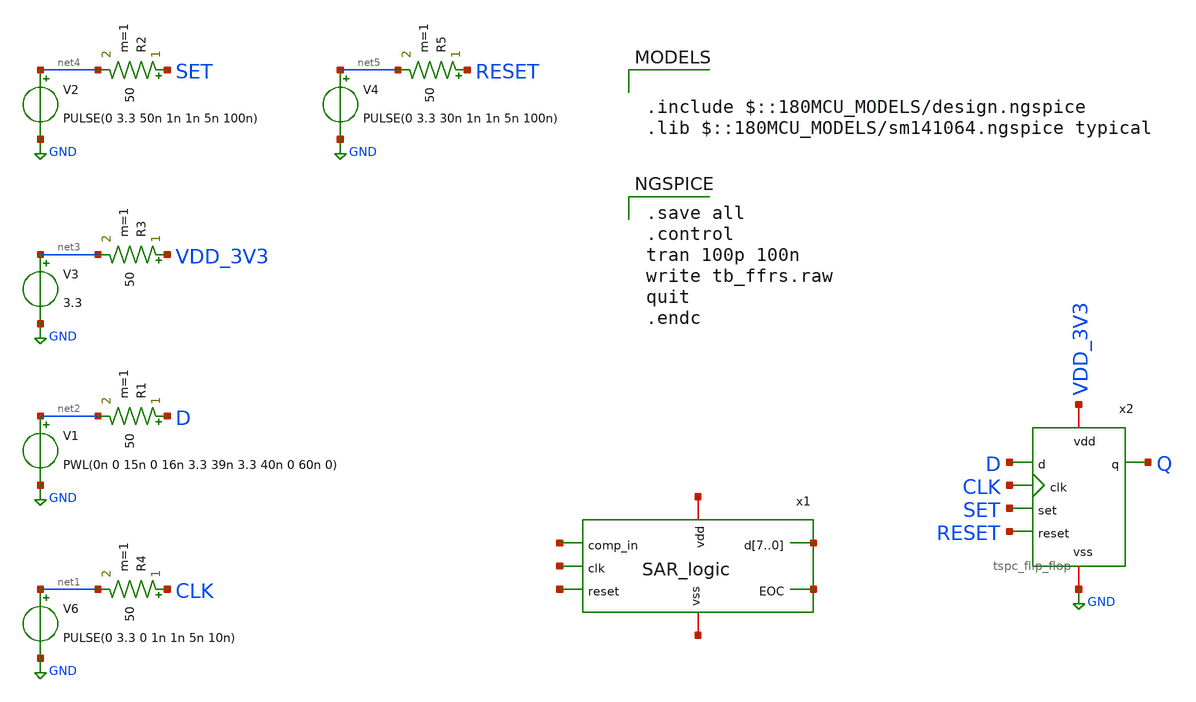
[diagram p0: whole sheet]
** sch_path: designs/libs/SAR_logic/SAR_logic_tb.sch
**.subckt SAR_logic_tb
V6 net1 GND PULSE(0 3.3 0 1n 1n 5n 10n)
R4 CLK net1 50 m=1
V1 net2 GND PWL(0n 0 15n 0 16n 3.3 39n 3.3 40n 0 60n 0)
R1 D net2 50 m=1
V3 net3 GND 3.3
R3 VDD_3V3 net3 50 m=1
V2 net4 GND PULSE(0 3.3 50n 1n 1n 5n 100n)
R2 SET net4 50 m=1
V4 net5 GND PULSE(0 3.3 30n 1n 1n 5n 100n)
R5 RESET net5 50 m=1
x2 VDD_3V3 GND D CLK SET RESET Q tspc_flip_flop
x1 net6 net7[7] net7[6] net7[5] net7[4] net7[3] net7[2] net7[1] net7[0] net8 net9 net10 net11 net12
+ SAR_logic
**** begin user architecture code

.include $::180MCU_MODELS/design.ngspice
.lib $::180MCU_MODELS/sm141064.ngspice typical


.save all
.control
tran 100p 100n
write tb_ffrs.raw
quit
.endc

**** end user architecture code
**.ends

* expanding   symbol:  libs/tspc_flip_flop/tspc_flip_flop.sym # of pins=7
** sym_path: designs/libs/tspc_flip_flop/tspc_flip_flop.sym
** sch_path: designs/libs/tspc_flip_flop/tspc_flip_flop.sch
.subckt tspc_flip_flop vdd vss d clk set reset q
*.iopin vdd
*.iopin vss
*.ipin d
*.ipin clk
*.ipin set
*.ipin reset
*.opin q
XM1 b1 d vss vss nfet_03v3 L=0.28u W=1u nf=1 ad='int((nf+1)/2) * W/nf * 0.18u' as='int((nf+2)/2) * W/nf * 0.18u'
+ pd='2*int((nf+1)/2) * (W/nf + 0.18u)' ps='2*int((nf+2)/2) * (W/nf + 0.18u)' nrd='0.18u / W' nrs='0.18u / W'
+ sa=0 sb=0 sd=0 m=1
XM2 b1 clk net1 net1 pfet_03v3 L=0.28u W=2u nf=1 ad='int((nf+1)/2) * W/nf * 0.18u' as='int((nf+2)/2) * W/nf * 0.18u'
+ pd='2*int((nf+1)/2) * (W/nf + 0.18u)' ps='2*int((nf+2)/2) * (W/nf + 0.18u)' nrd='0.18u / W' nrs='0.18u / W'
+ sa=0 sb=0 sd=0 m=1
XM3 net1 d vdd vdd pfet_03v3 L=0.28u W=2u nf=1 ad='int((nf+1)/2) * W/nf * 0.18u' as='int((nf+2)/2) * W/nf * 0.18u'
+ pd='2*int((nf+1)/2) * (W/nf + 0.18u)' ps='2*int((nf+2)/2) * (W/nf + 0.18u)' nrd='0.18u / W' nrs='0.18u / W'
+ sa=0 sb=0 sd=0 m=1
XM4 b2 clk vdd vdd pfet_03v3 L=0.28u W=2u nf=1 ad='int((nf+1)/2) * W/nf * 0.18u' as='int((nf+2)/2) * W/nf * 0.18u'
+ pd='2*int((nf+1)/2) * (W/nf + 0.18u)' ps='2*int((nf+2)/2) * (W/nf + 0.18u)' nrd='0.18u / W' nrs='0.18u / W'
+ sa=0 sb=0 sd=0 m=1
XM5 b2 b1 net2 vss nfet_03v3 L=0.28u W=1u nf=1 ad='int((nf+1)/2) * W/nf * 0.18u' as='int((nf+2)/2) * W/nf * 0.18u'
+ pd='2*int((nf+1)/2) * (W/nf + 0.18u)' ps='2*int((nf+2)/2) * (W/nf + 0.18u)' nrd='0.18u / W' nrs='0.18u / W'
+ sa=0 sb=0 sd=0 m=1
XM6 net2 clk vss vss nfet_03v3 L=0.28u W=1u nf=1 ad='int((nf+1)/2) * W/nf * 0.18u' as='int((nf+2)/2) * W/nf * 0.18u'
+ pd='2*int((nf+1)/2) * (W/nf + 0.18u)' ps='2*int((nf+2)/2) * (W/nf + 0.18u)' nrd='0.18u / W' nrs='0.18u / W'
+ sa=0 sb=0 sd=0 m=1
XM7 net4 b2 vss vss nfet_03v3 L=0.28u W=1u nf=1 ad='int((nf+1)/2) * W/nf * 0.18u' as='int((nf+2)/2) * W/nf * 0.18u'
+ pd='2*int((nf+1)/2) * (W/nf + 0.18u)' ps='2*int((nf+2)/2) * (W/nf + 0.18u)' nrd='0.18u / W' nrs='0.18u / W'
+ sa=0 sb=0 sd=0 m=1
XM8 b3 clk net4 vss nfet_03v3 L=0.28u W=1u nf=1 ad='int((nf+1)/2) * W/nf * 0.18u' as='int((nf+2)/2) * W/nf * 0.18u'
+ pd='2*int((nf+1)/2) * (W/nf + 0.18u)' ps='2*int((nf+2)/2) * (W/nf + 0.18u)' nrd='0.18u / W' nrs='0.18u / W'
+ sa=0 sb=0 sd=0 m=1
XM9 b3 set net3 net3 pfet_03v3 L=0.28u W=2u nf=1 ad='int((nf+1)/2) * W/nf * 0.18u' as='int((nf+2)/2) * W/nf * 0.18u'
+ pd='2*int((nf+1)/2) * (W/nf + 0.18u)' ps='2*int((nf+2)/2) * (W/nf + 0.18u)' nrd='0.18u / W' nrs='0.18u / W'
+ sa=0 sb=0 sd=0 m=1
XM10 net3 b2 vdd vdd pfet_03v3 L=0.28u W=2u nf=1 ad='int((nf+1)/2) * W/nf * 0.18u' as='int((nf+2)/2) * W/nf * 0.18u'
+ pd='2*int((nf+1)/2) * (W/nf + 0.18u)' ps='2*int((nf+2)/2) * (W/nf + 0.18u)' nrd='0.18u / W' nrs='0.18u / W'
+ sa=0 sb=0 sd=0 m=1
XM11 b3 net5 vdd vdd pfet_03v3 L=0.28u W=2u nf=1 ad='int((nf+1)/2) * W/nf * 0.18u' as='int((nf+2)/2) * W/nf * 0.18u'
+ pd='2*int((nf+1)/2) * (W/nf + 0.18u)' ps='2*int((nf+2)/2) * (W/nf + 0.18u)' nrd='0.18u / W' nrs='0.18u / W'
+ sa=0 sb=0 sd=0 m=1
XM12 b3 set vss vss nfet_03v3 L=0.28u W=1u nf=1 ad='int((nf+1)/2) * W/nf * 0.18u' as='int((nf+2)/2) * W/nf * 0.18u'
+ pd='2*int((nf+1)/2) * (W/nf + 0.18u)' ps='2*int((nf+2)/2) * (W/nf + 0.18u)' nrd='0.18u / W' nrs='0.18u / W'
+ sa=0 sb=0 sd=0 m=1
XM13 q b3 vdd vdd pfet_03v3 L=0.28u W=2u nf=1 ad='int((nf+1)/2) * W/nf * 0.18u' as='int((nf+2)/2) * W/nf * 0.18u'
+ pd='2*int((nf+1)/2) * (W/nf + 0.18u)' ps='2*int((nf+2)/2) * (W/nf + 0.18u)' nrd='0.18u / W' nrs='0.18u / W'
+ sa=0 sb=0 sd=0 m=1
XM14 q b3 vss vss nfet_03v3 L=0.28u W=1u nf=1 ad='int((nf+1)/2) * W/nf * 0.18u' as='int((nf+2)/2) * W/nf * 0.18u'
+ pd='2*int((nf+1)/2) * (W/nf + 0.18u)' ps='2*int((nf+2)/2) * (W/nf + 0.18u)' nrd='0.18u / W' nrs='0.18u / W'
+ sa=0 sb=0 sd=0 m=1
XM15 net5 reset vdd vdd pfet_03v3 L=0.28u W=2u nf=1 ad='int((nf+1)/2) * W/nf * 0.18u' as='int((nf+2)/2) * W/nf * 0.18u'
+ pd='2*int((nf+1)/2) * (W/nf + 0.18u)' ps='2*int((nf+2)/2) * (W/nf + 0.18u)' nrd='0.18u / W' nrs='0.18u / W'
+ sa=0 sb=0 sd=0 m=1
XM16 net5 reset vss vss nfet_03v3 L=0.28u W=1u nf=1 ad='int((nf+1)/2) * W/nf * 0.18u' as='int((nf+2)/2) * W/nf * 0.18u'
+ pd='2*int((nf+1)/2) * (W/nf + 0.18u)' ps='2*int((nf+2)/2) * (W/nf + 0.18u)' nrd='0.18u / W' nrs='0.18u / W'
+ sa=0 sb=0 sd=0 m=1
.ends


* expanding   symbol:  libs/SAR_logic/SAR_logic.sym # of pins=7
** sym_path: designs/libs/SAR_logic/SAR_logic.sym
** sch_path: designs/libs/SAR_logic/SAR_logic.sch
.subckt SAR_logic comp_in d7 d6 d5 d4 d3 d2 d1 d0 EOC clk reset vdd vss
*.ipin comp_in
*.iopin vdd
*.iopin vss
*.ipin clk
*.ipin reset
*.opin d7,d6,d5,d4,d3,d2,d1,d0
*.opin EOC
x1 vdd vss EOC clk reset net1 net2 tspc_flip_flop
* noconn #net1
x2 vdd vss net2 clk net3 reset net4 tspc_flip_flop
* noconn #net3
x3 vdd vss net4 clk net5 reset net6 tspc_flip_flop
* noconn #net5
x4 vdd vss net6 clk net7 reset net8 tspc_flip_flop
* noconn #net7
x5 vdd vss net8 clk net9 reset net10 tspc_flip_flop
* noconn #net9
x6 vdd vss net10 clk net11 reset net12 tspc_flip_flop
* noconn #net11
x7 vdd vss net12 clk net13 reset net14 tspc_flip_flop
* noconn #net13
x8 vdd vss net14 clk net15 reset net16 tspc_flip_flop
* noconn #net15
x9 vdd vss net16 clk net17 reset net18 tspc_flip_flop
* noconn #net17
x10 vdd vss net18 clk net19 reset EOC tspc_flip_flop
* noconn #net19
x11 vdd vss comp_in d6 net4 reset d7 tspc_flip_flop
x12 vdd vss comp_in d5 net6 reset d6 tspc_flip_flop
x13 vdd vss comp_in d4 net8 reset d5 tspc_flip_flop
x14 vdd vss comp_in d3 net10 reset d4 tspc_flip_flop
x15 vdd vss comp_in d2 net12 reset d3 tspc_flip_flop
x16 vdd vss comp_in d1 net14 reset d2 tspc_flip_flop
x17 vdd vss comp_in d0 net16 reset d1 tspc_flip_flop
x18 vdd vss comp_in net20 net18 reset d0 tspc_flip_flop
x19 vdd vss vss vss EOC reset net20 tspc_flip_flop
.ends

.GLOBAL GND
.end
